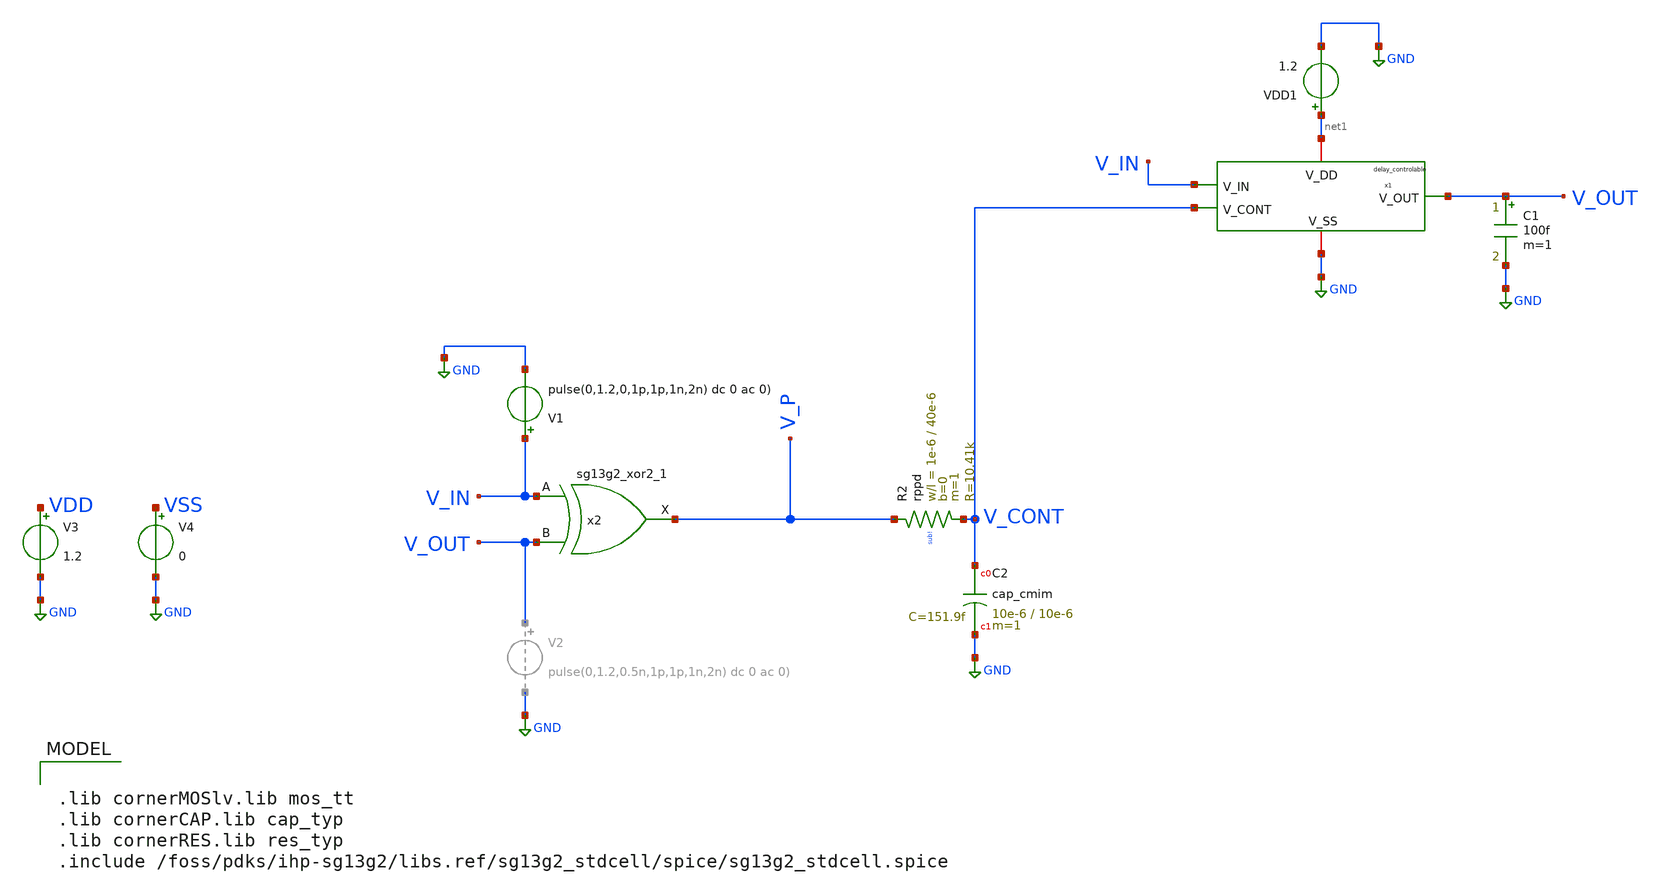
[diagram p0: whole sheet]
** sch_path: others/probe_top.sch
**.subckt probe_top
VDD1 net1 GND 1.2
C1 V_OUT GND 100f m=1
x1 net1 V_OUT V_IN V_CONT GND delay_controlable
V1 V_IN GND pulse(0,1.2,0,1p,1p,1n,2n) dc 0 ac 0)
x2 V_P V_IN V_OUT VDD VSS sg13g2_xor2_1
V3 VDD GND 1.2
V4 VSS GND 0
XC2 V_CONT GND cap_cmim w=10e-6 l=10e-6 m=1 mm_ok=1
XR2 V_P V_CONT sub! rppd w=1e-6 l=40e-6 m=1 b=0 mm_ok=1
**** begin user architecture code

.lib cornerMOSlv.lib mos_tt
.lib cornerCAP.lib cap_typ
.lib cornerRES.lib res_typ
.include /foss/pdks/ihp-sg13g2/libs.ref/sg13g2_stdcell/spice/sg13g2_stdcell.spice



.control
* ---- settings you tweak ----


   * ---- user settings ----
  let vlow  = 0
  let vhigh = 1.2
  let v50   = vlow + 0.5*(vhigh - vlow)

  let start_edge = 0     ; skip early edges (settling)
  let N = 1000             ; number of phase samples



  tran 1p 1000n

  * ---- allocate vectors ----
  let tvec   = vector(N)
  let phivec = vector(N)

  let k = 0
  let i = start_edge

  while k < N
    * crossing times
    meas tran tin      WHEN v(v_in)=v50  RISE=i
    meas tran tout     WHEN v(v_out)=v50 RISE=i
    meas tran tin_next WHEN v(v_in)=v50  RISE=(i+1)

    * delay + period
    let dt = tout - tin
    let T  = tin_next - tin

    * phase in degrees (per-cycle)
    let phi = 360*dt/T
    let phi = phi - 360*floor(phi/360)

    * store sample at time = tin
    let tvec[k]   = tin
    let phivec[k] = phi

    let k = k + 1
    let i = i + 1
  end

  * plot phase vs time (one point per cycle)
  plot phivec vs tvec
  plot v(V_CONT) V_P
  plot v(V_IN) v(V_OUT) v(V_CONT)
.endc


**** end user architecture code
**.ends

* expanding   symbol:  /foss/designs/DLL/2026/clemen/delay_controlable.sym # of pins=5
** sym_path: others/clemen/delay_controlable.sym
** sch_path: others/clemen/delay_controlable.sch
.subckt delay_controlable V_DD V_OUT V_IN V_CONT V_SS
*.iopin V_DD
*.iopin V_SS
*.ipin V_IN
*.ipin V_CONT
*.opin V_OUT
XM1 V_OUT V_IN net3 V_SS sg13_lv_nmos w=2u l=0.13u ng=1 m=1 mm_ok=1
XM2 net3 V_CONT V_SS V_SS sg13_lv_nmos w=5u l=0.16u ng=1 m=1 mm_ok=1
XM3 net1 V_CONT V_SS V_SS sg13_lv_nmos w=2u l=0.25u ng=1 m=1 mm_ok=1
XM4 V_OUT V_IN net2 V_DD sg13_lv_pmos w=5u l=0.13u ng=1 m=1 mm_ok=1
XM5 net2 net1 V_DD V_DD sg13_lv_pmos w=5u l=0.16u ng=1 m=1 mm_ok=1
XM6 net1 net1 V_DD V_DD sg13_lv_pmos w=2.24u l=0.13u ng=1 m=1 mm_ok=1
.ends


* expanding   symbol:  sg13g2_stdcells/sg13g2_xor2_1.sym # of pins=3
** sym_path: sg13g2_stdcells/sg13g2_xor2_1.sym
** sch_path: sg13g2_stdcells/sg13g2_xor2_1.sch
.subckt sg13g2_xor2_1 X A B VDD VSS
*.opin X
*.ipin B
*.ipin A
*.iopin VDD
*.iopin VSS
XM1 net1 A VSS VSS sg13_lv_nmos w=550.00n l=130.00n ng=1 m=1 mm_ok=1
XM2 net1 B VSS VSS sg13_lv_nmos w=550.00n l=130.00n ng=1 m=1 mm_ok=1
XM3 X net1 VSS VSS sg13_lv_nmos w=740.00n l=130.00n ng=1 m=1 mm_ok=1
XM4 X B net3 VSS sg13_lv_nmos w=740.00n l=130.00n ng=1 m=1 mm_ok=1
XM5 net3 A VSS VSS sg13_lv_nmos w=740.00n l=130.00n ng=1 m=1 mm_ok=1
XM6 net4 A VDD VDD sg13_lv_pmos w=1.000u l=130.00n ng=1 m=1 mm_ok=1
XM7 net1 B net4 VDD sg13_lv_pmos w=1.000u l=130.00n ng=1 m=1 mm_ok=1
XM8 net2 A VDD VDD sg13_lv_pmos w=1.12u l=130.00n ng=1 m=1 mm_ok=1
XM9 X net1 net2 VDD sg13_lv_pmos w=1.12u l=130.00n ng=1 m=1 mm_ok=1
XM10 net2 B VDD VDD sg13_lv_pmos w=1.12u l=130.00n ng=1 m=1 mm_ok=1
.ends

.GLOBAL GND
.end
